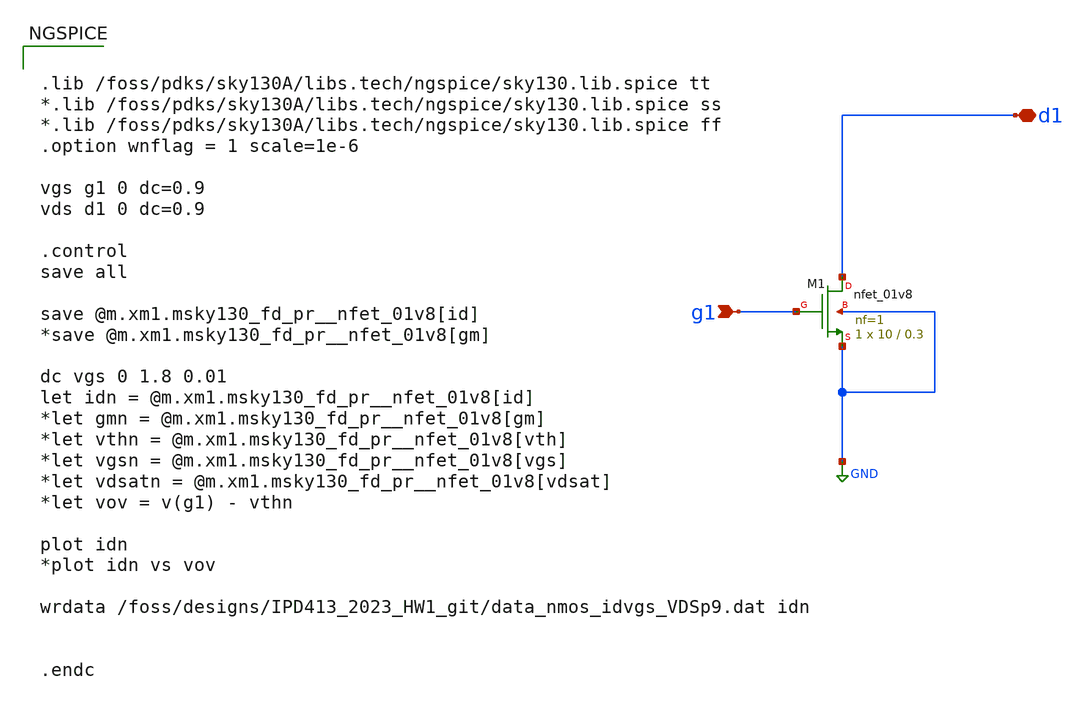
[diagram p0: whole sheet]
** sch_path: nmos_charac_IPD413HW1.sch
**.subckt nmos_charac_IPD413HW1 g1 d1
*.ipin g1
*.iopin d1
XM1 d1 g1 GND GND sky130_fd_pr__nfet_01v8 L=0.3 W=10 nf=1 ad='int((nf+1)/2) * W/nf * 0.29' as='int((nf+2)/2) * W/nf * 0.29'
+ pd='2*int((nf+1)/2) * (W/nf + 0.29)' ps='2*int((nf+2)/2) * (W/nf + 0.29)' nrd='0.29 / W' nrs='0.29 / W'
+ sa=0 sb=0 sd=0 mult=1 m=1
**** begin user architecture code


.lib /foss/pdks/sky130A/libs.tech/ngspice/sky130.lib.spice tt
*.lib /foss/pdks/sky130A/libs.tech/ngspice/sky130.lib.spice ss
*.lib /foss/pdks/sky130A/libs.tech/ngspice/sky130.lib.spice ff
.option wnflag = 1 scale=1e-6

vgs g1 0 dc=0.9
vds d1 0 dc=0.9

.control
save all

save @m.xm1.msky130_fd_pr__nfet_01v8[id]
*save @m.xm1.msky130_fd_pr__nfet_01v8[gm]

dc vgs 0 1.8 0.01
let idn = @m.xm1.msky130_fd_pr__nfet_01v8[id]
*let gmn = @m.xm1.msky130_fd_pr__nfet_01v8[gm]
*let vthn = @m.xm1.msky130_fd_pr__nfet_01v8[vth]
*let vgsn = @m.xm1.msky130_fd_pr__nfet_01v8[vgs]
*let vdsatn = @m.xm1.msky130_fd_pr__nfet_01v8[vdsat]
*let vov = v(g1) - vthn

plot idn
*plot idn vs vov

wrdata /foss/designs/IPD413_2023_HW1_git/data_nmos_idvgs_VDSp9.dat idn


.endc


**** end user architecture code
**.ends
.GLOBAL GND
.end
